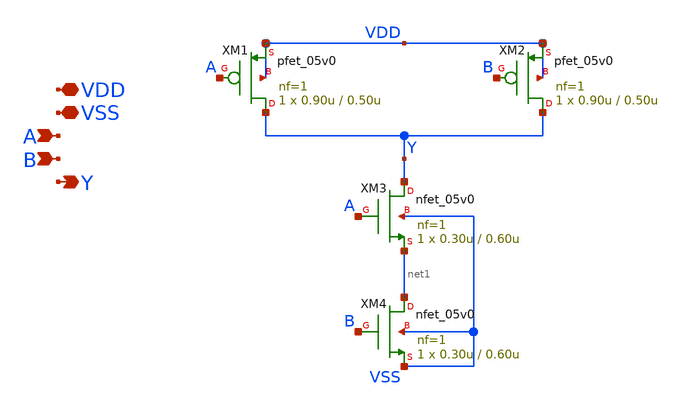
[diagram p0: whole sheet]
** sch_path: xschem/switch-matrix/nand2_1.sch
**.subckt nand2_1 VDD VSS A B Y
*.iopin VDD
*.iopin VSS
*.ipin A
*.ipin B
*.opin Y
XM1 Y A VDD VDD pfet_05v0 L=0.50u W=0.90u nf=1 ad='int((nf+1)/2) * W/nf * 0.18u' as='int((nf+2)/2) * W/nf * 0.18u'
+ pd='2*int((nf+1)/2) * (W/nf + 0.18u)' ps='2*int((nf+2)/2) * (W/nf + 0.18u)' nrd='0.18u / W' nrs='0.18u / W'
+ sa=0 sb=0 sd=0 m=1
XM2 Y B VDD VDD pfet_05v0 L=0.50u W=0.90u nf=1 ad='int((nf+1)/2) * W/nf * 0.18u' as='int((nf+2)/2) * W/nf * 0.18u'
+ pd='2*int((nf+1)/2) * (W/nf + 0.18u)' ps='2*int((nf+2)/2) * (W/nf + 0.18u)' nrd='0.18u / W' nrs='0.18u / W'
+ sa=0 sb=0 sd=0 m=1
XM3 Y A net1 VSS nfet_05v0 L=0.60u W=0.30u nf=1 ad='int((nf+1)/2) * W/nf * 0.18u' as='int((nf+2)/2) * W/nf * 0.18u'
+ pd='2*int((nf+1)/2) * (W/nf + 0.18u)' ps='2*int((nf+2)/2) * (W/nf + 0.18u)' nrd='0.18u / W' nrs='0.18u / W'
+ sa=0 sb=0 sd=0 m=1
XM4 net1 B VSS VSS nfet_05v0 L=0.60u W=0.30u nf=1 ad='int((nf+1)/2) * W/nf * 0.18u' as='int((nf+2)/2) * W/nf * 0.18u'
+ pd='2*int((nf+1)/2) * (W/nf + 0.18u)' ps='2*int((nf+2)/2) * (W/nf + 0.18u)' nrd='0.18u / W' nrs='0.18u / W'
+ sa=0 sb=0 sd=0 m=1
**.ends
.end
